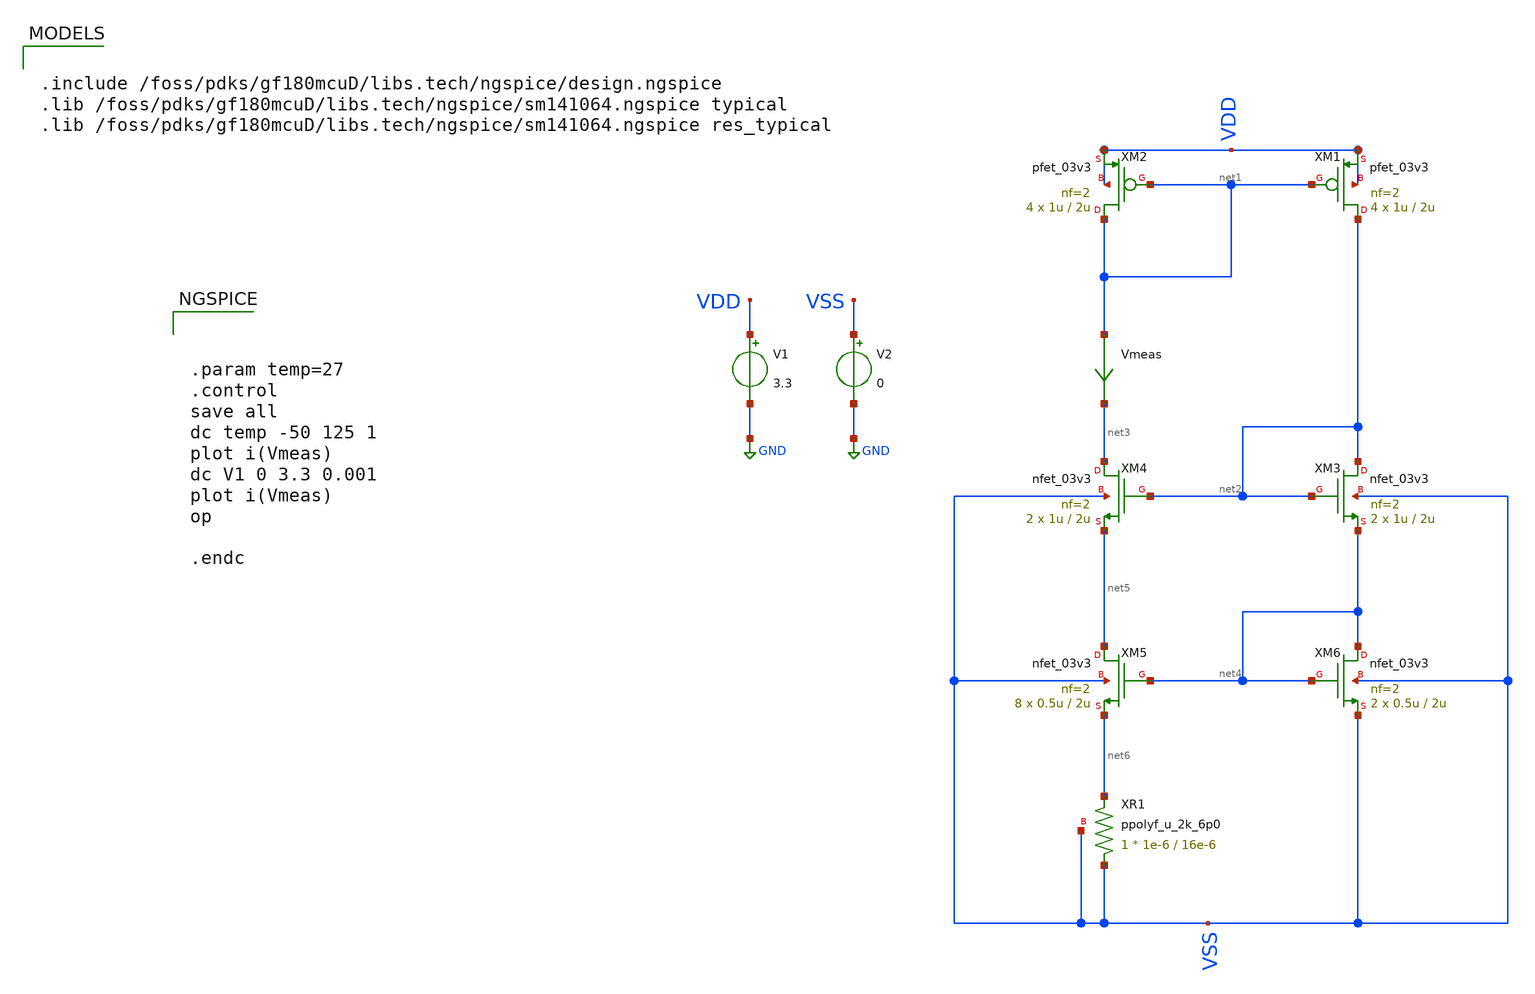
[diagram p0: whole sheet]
** sch_path: Learning/single_ended_amplifiers/VA001_series/Design_and_Analysis_of_Two-Stage_CMOS_Operational_Amplifier_for_Fluorescence_Signal_Processing_gf180mcu_3_3V/transcondutance/tb.sch
**.subckt tb
Vmeas net1 net3 0
.save i(vmeas)
V1 VDD GND 3.3
V2 VSS GND 0
XR1 VSS net6 VSS ppolyf_u_2k_6p0 r_width=1e-6 r_length=16e-6 m=1
XM2 net1 net1 VDD VDD pfet_03v3 L=2u W=1u nf=2 ad='int((nf+1)/2) * W/nf * 0.18u' as='int((nf+2)/2) * W/nf * 0.18u'
+ pd='2*int((nf+1)/2) * (W/nf + 0.18u)' ps='2*int((nf+2)/2) * (W/nf + 0.18u)' nrd='0.18u / W' nrs='0.18u / W'
+ sa=0 sb=0 sd=0 m=4
XM4 net3 net2 net5 VSS nfet_03v3 L=2u W=1u nf=2 ad='int((nf+1)/2) * W/nf * 0.18u' as='int((nf+2)/2) * W/nf * 0.18u'
+ pd='2*int((nf+1)/2) * (W/nf + 0.18u)' ps='2*int((nf+2)/2) * (W/nf + 0.18u)' nrd='0.18u / W' nrs='0.18u / W'
+ sa=0 sb=0 sd=0 m=2
XM5 net5 net4 net6 VSS nfet_03v3 L=2u W=0.5u nf=2 ad='int((nf+1)/2) * W/nf * 0.18u' as='int((nf+2)/2) * W/nf * 0.18u'
+ pd='2*int((nf+1)/2) * (W/nf + 0.18u)' ps='2*int((nf+2)/2) * (W/nf + 0.18u)' nrd='0.18u / W' nrs='0.18u / W'
+ sa=0 sb=0 sd=0 m=8
XM6 net4 net4 VSS VSS nfet_03v3 L=2u W=0.5u nf=2 ad='int((nf+1)/2) * W/nf * 0.18u' as='int((nf+2)/2) * W/nf * 0.18u'
+ pd='2*int((nf+1)/2) * (W/nf + 0.18u)' ps='2*int((nf+2)/2) * (W/nf + 0.18u)' nrd='0.18u / W' nrs='0.18u / W'
+ sa=0 sb=0 sd=0 m=2
XM3 net2 net2 net4 VSS nfet_03v3 L=2u W=1u nf=2 ad='int((nf+1)/2) * W/nf * 0.18u' as='int((nf+2)/2) * W/nf * 0.18u'
+ pd='2*int((nf+1)/2) * (W/nf + 0.18u)' ps='2*int((nf+2)/2) * (W/nf + 0.18u)' nrd='0.18u / W' nrs='0.18u / W'
+ sa=0 sb=0 sd=0 m=2
XM1 net2 net1 VDD VDD pfet_03v3 L=2u W=1u nf=2 ad='int((nf+1)/2) * W/nf * 0.18u' as='int((nf+2)/2) * W/nf * 0.18u'
+ pd='2*int((nf+1)/2) * (W/nf + 0.18u)' ps='2*int((nf+2)/2) * (W/nf + 0.18u)' nrd='0.18u / W' nrs='0.18u / W'
+ sa=0 sb=0 sd=0 m=4
**** begin user architecture code

.include /foss/pdks/gf180mcuD/libs.tech/ngspice/design.ngspice
.lib /foss/pdks/gf180mcuD/libs.tech/ngspice/sm141064.ngspice typical
.lib /foss/pdks/gf180mcuD/libs.tech/ngspice/sm141064.ngspice res_typical

**** end user architecture code
**.ends
.GLOBAL GND
**** begin user architecture code



.param temp=27
.control
save all
dc temp -50 125 1
plot i(Vmeas)
dc V1 0 3.3 0.001
plot i(Vmeas)
op

.endc


**** end user architecture code
.end
